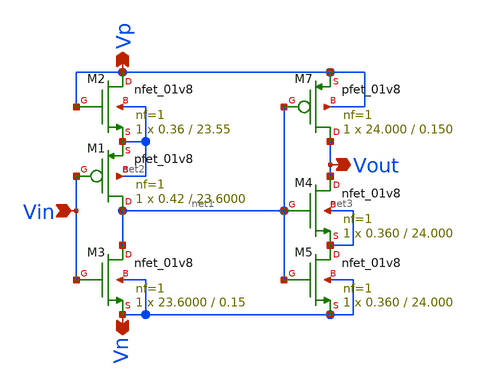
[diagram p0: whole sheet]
** sch_path: xschem/Vth_sch/Symbol/th02.sch
**.subckt th02 Vn Vp Vin Vout
*.opin Vn
*.opin Vp
*.ipin Vin
*.opin Vout
XM7 Vout net1 Vp Vp sky130_fd_pr__pfet_01v8 L=0.150 W=24.000 nf=1 ad='int((nf+1)/2) * W/nf * 0.29' as='int((nf+2)/2) * W/nf * 0.29'
+ pd='2*int((nf+1)/2) * (W/nf + 0.29)' ps='2*int((nf+2)/2) * (W/nf + 0.29)' nrd='0.29 / W' nrs='0.29 / W'
+ sa=0 sb=0 sd=0 mult=1 m=1
XM1 net1 Vin net2 net2 sky130_fd_pr__pfet_01v8 L=23.6000 W=0.42 nf=1 ad='int((nf+1)/2) * W/nf * 0.29'
+ as='int((nf+2)/2) * W/nf * 0.29' pd='2*int((nf+1)/2) * (W/nf + 0.29)' ps='2*int((nf+2)/2) * (W/nf + 0.29)'
+ nrd='0.29 / W' nrs='0.29 / W' sa=0 sb=0 sd=0 mult=1 m=1
XM3 net1 Vin Vn Vn sky130_fd_pr__nfet_01v8 L=0.15 W=23.6000 nf=1 ad='int((nf+1)/2) * W/nf * 0.29' as='int((nf+2)/2) * W/nf * 0.29'
+ pd='2*int((nf+1)/2) * (W/nf + 0.29)' ps='2*int((nf+2)/2) * (W/nf + 0.29)' nrd='0.29 / W' nrs='0.29 / W'
+ sa=0 sb=0 sd=0 mult=1 m=1
XM2 Vp Vp net2 net2 sky130_fd_pr__nfet_01v8 L=23.55 W=0.36 nf=1 ad='int((nf+1)/2) * W/nf * 0.29' as='int((nf+2)/2) * W/nf * 0.29'
+ pd='2*int((nf+1)/2) * (W/nf + 0.29)' ps='2*int((nf+2)/2) * (W/nf + 0.29)' nrd='0.29 / W' nrs='0.29 / W'
+ sa=0 sb=0 sd=0 mult=1 m=1
XM4 Vout net1 net3 net3 sky130_fd_pr__nfet_01v8 L=24.000 W=0.360 nf=1 ad='int((nf+1)/2) * W/nf * 0.29'
+ as='int((nf+2)/2) * W/nf * 0.29' pd='2*int((nf+1)/2) * (W/nf + 0.29)' ps='2*int((nf+2)/2) * (W/nf + 0.29)'
+ nrd='0.29 / W' nrs='0.29 / W' sa=0 sb=0 sd=0 mult=1 m=1
XM5 net3 net1 Vn Vn sky130_fd_pr__nfet_01v8 L=24.000 W=0.360 nf=1 ad='int((nf+1)/2) * W/nf * 0.29' as='int((nf+2)/2) * W/nf * 0.29'
+ pd='2*int((nf+1)/2) * (W/nf + 0.29)' ps='2*int((nf+2)/2) * (W/nf + 0.29)' nrd='0.29 / W' nrs='0.29 / W'
+ sa=0 sb=0 sd=0 mult=1 m=1
**.ends
.end
